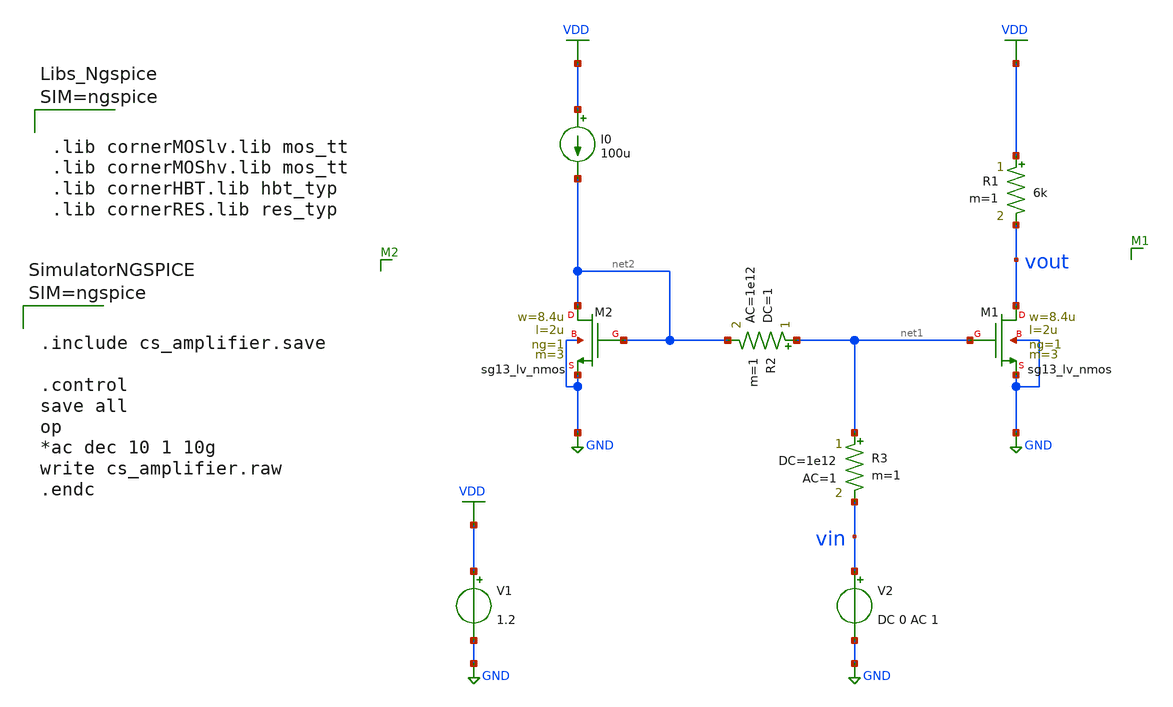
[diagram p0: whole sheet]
** sch_path: Schematics/lab_1/cs_amplifier.sch
**.subckt cs_amplifier
XM1 vout net1 GND GND sg13_lv_nmos w=8.4u l=2u ng=1 m=3 mm_ok=1
R1 VDD vout 6k m=1
I0 VDD net2 100u
R2 net1 net2 1 ac=1e12 m=1
XM2 net2 net2 GND GND sg13_lv_nmos w=8.4u l=2u ng=1 m=3 mm_ok=1
R3 net1 vin 1e12 ac=1 m=1
V1 VDD GND 1.2
V2 vin GND DC 0 AC 1
**** begin user architecture code



.lib cornerMOSlv.lib mos_tt
.lib cornerMOShv.lib mos_tt
.lib cornerHBT.lib hbt_typ
.lib cornerRES.lib res_typ






.include cs_amplifier.save

.control
save all
op
*ac dec 10 1 10g
write cs_amplifier.raw
.endc



**** end user architecture code
**.ends
.GLOBAL GND
.GLOBAL VDD
.end
